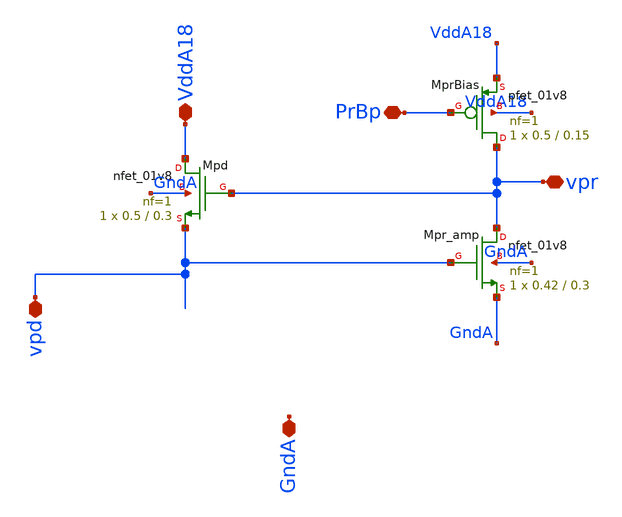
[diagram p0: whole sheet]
** sch_path: analog/xschem/PixelPhotoreceptor.sch
**.subckt PixelPhotoreceptor PrBp VddA18 vpd GndA vpr
*.iopin PrBp
*.iopin VddA18
*.iopin vpd
*.iopin GndA
*.iopin vpr
XMpd VddA18 vpr vpd GndA sky130_fd_pr__nfet_01v8 L=0.3 W=0.5 nf=1 ad='int((1 + 1)/2) * 0.5 / 1 * 0.29'
+ as='int((1 + 2)/2) * 0.5 / 1 * 0.29' pd='2*int((1 + 1)/2) * (0.5 / 1 + 0.29)' ps='2*int((1 + 2)/2) * (0.5 / 1 + 0.29)'
+ nrd='0.29 / 0.5 ' nrs='0.29 / 0.5 ' sa=0 sb=0 sd=0 mult=1 m=1
XMpr_amp vpr vpd GndA GndA sky130_fd_pr__nfet_01v8 L=0.3 W=0.42 nf=1 ad='int((1 + 1)/2) * 0.42 / 1 * 0.29'
+ as='int((1 + 2)/2) * 0.42 / 1 * 0.29' pd='2*int((1 + 1)/2) * (0.42 / 1 + 0.29)' ps='2*int((1 + 2)/2) * (0.42 / 1 + 0.29)'
+ nrd='0.29 / 0.42 ' nrs='0.29 / 0.42 ' sa=0 sb=0 sd=0 mult=1 m=1
XMprBias vpr PrBp VddA18 VddA18 sky130_fd_pr__pfet_01v8 L=0.15 W=0.5 nf=1 ad=150e-3 as=150e-3 pd=1.6
+ ps=1.6 nrd='0.29 / 0.5 ' nrs='0.29 / 0.5 ' sa=0 sb=0 sd=0 mult=1 m=1
**.ends
.end
